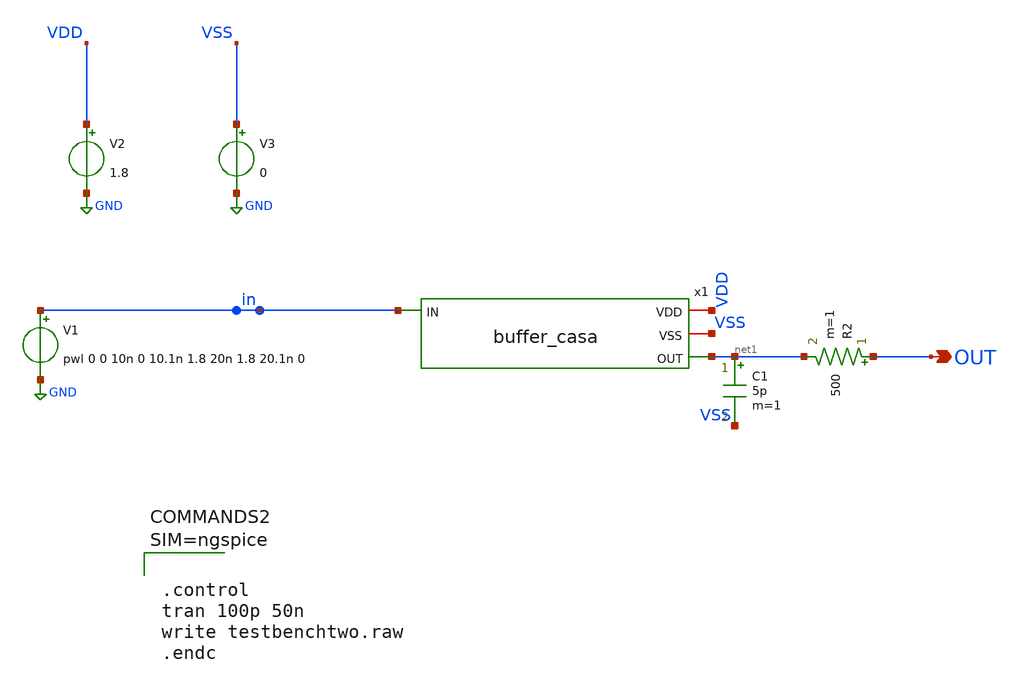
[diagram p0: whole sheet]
** sch_path: xschem/testbench_casa.sch
**.subckt testbench_casa OUT
*.opin OUT
x1 VDD VSS net1 in buffer_casa
V2 VDD GND 1.8
V3 VSS GND 0
V1 in GND pwl 0 0 10n 0 10.1n 1.8 20n 1.8 20.1n 0
R2 OUT net1 500 m=1
C1 net1 VSS 5p m=1
**** begin user architecture code

** opencircuitdesign pdks install
.lib $::SKYWATER_MODELS/sky130.lib.spice tt





.control
tran 100p 50n
write testbenchtwo.raw
.endc



**** end user architecture code
**.ends
.GLOBAL GND
.end
